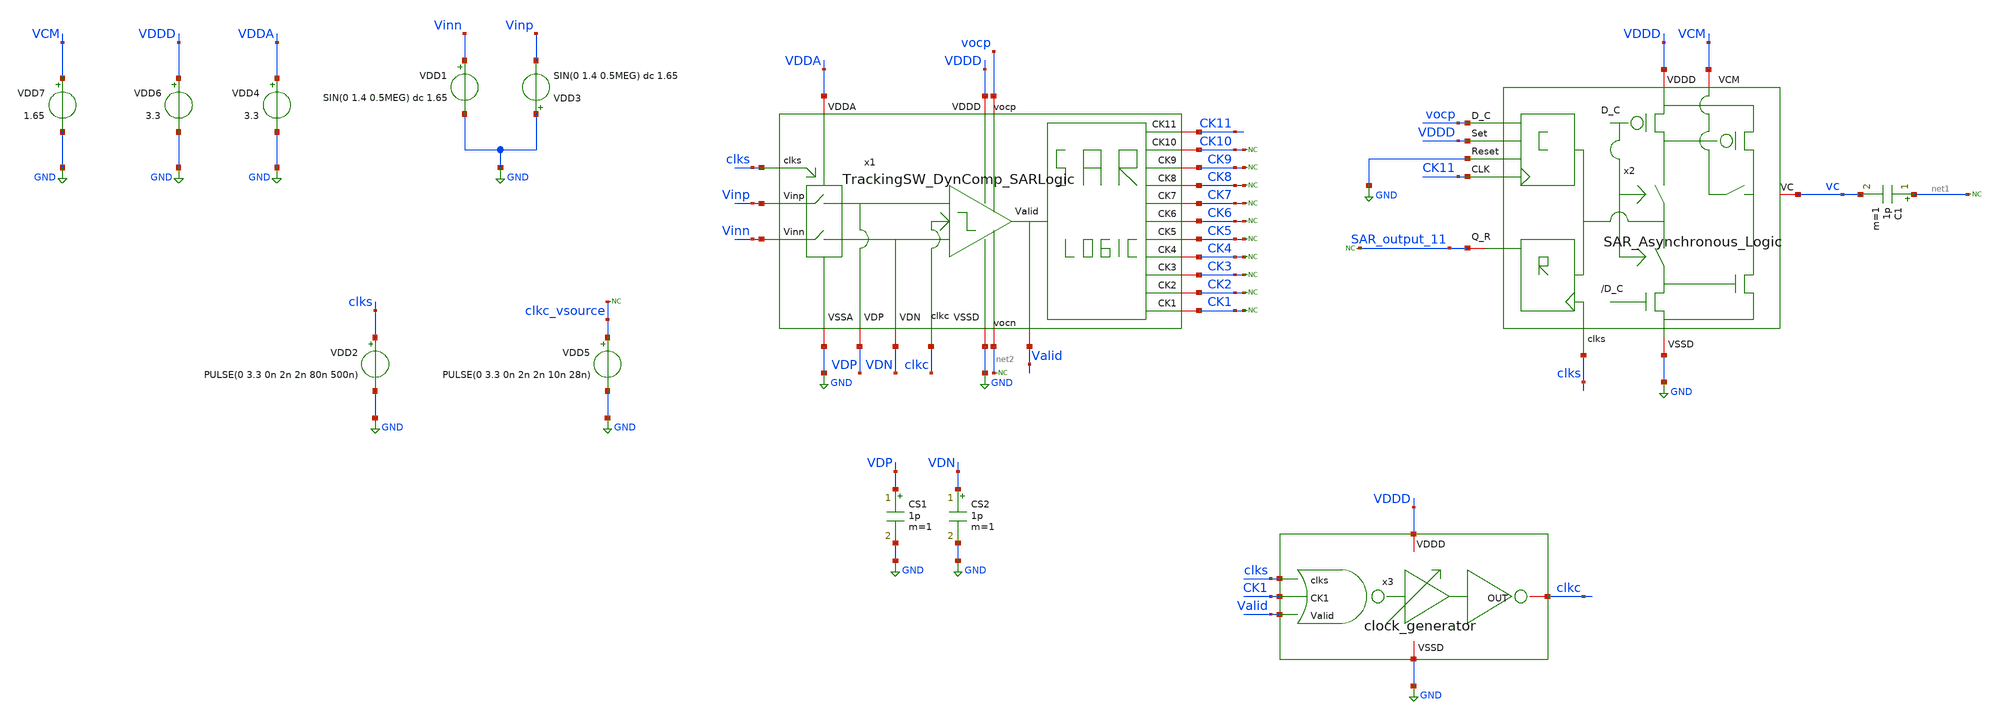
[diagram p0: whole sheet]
** sch_path: SAR_ADC/SAR_Asynchronous_Logic/xschem/SAR_Asynchronous_Logic_tb_ckp.sch
**.subckt SAR_Asynchronous_Logic_tb_ckp
VDD2 clks GND PULSE(0 3.3 0n 2n 2n 80n 500n)
VDD4 VDDA GND 3.3
VDD1 Vinn GND SIN(0 1.4 0.5MEG) dc 1.65
VDD3 GND Vinp SIN(0 1.4 0.5MEG) dc 1.65
VDD5 clkc_vsource GND PULSE(0 3.3 0n 2n 2n 10n 28n)
VDD6 VDDD GND 3.3
CS1 VDP GND 1p m=1
CS2 VDN GND 1p m=1
* noconn CK10
* noconn CK9
* noconn CK8
* noconn CK7
* noconn CK6
* noconn CK5
* noconn CK4
* noconn CK3
* noconn CK2
* noconn CK1
VDD7 VCM GND 1.65
x2 VCM vc SAR_output_11 clks VDDD GND VDDD GND vocp CK11 SAR_Asynchronous_Logic
* noconn #net1
* noconn #net2
x3 clkc VDDD GND clks CK1 Valid clock_generator
* noconn clkc_vsource
* noconn SAR_output_11
x1 Valid vocp net2 CK11 CK10 CK9 CK8 CK7 CK6 CK5 CK4 CK3 CK2 CK1 VDDA GND VDDD GND VDP clks VDN clkc
+ Vinp Vinn TrackingSW_DynComp_SARLogic
C1 net1 vc 1p m=1
**** begin user architecture code



*Parameters

.options TEMP = 50.0
.lib /home/electrica/Documents/gf180_projects/pdk/gf180mcuC/libs.tech/ngspice/sm141064.ngspice typical
.include /home/electrica/Documents/gf180_projects/pdk/gf180mcuC/libs.tech/ngspice/design.ngspice

*Data to save
.save all


* Simulation
.control
tran 0.1n 5u 0.01n
*setplot dc1
plot V(clkc_vsource)+16 V(clkc)+12 V(CK11)+8 V(vocp)+4 V(vc)
set filetype = ascii
write SAR_Asynchronous_Logic_tb_tran.raw

reset
unset filetype
op
save all
write SAR_Asynchronous_Logic_tb.raw


.endc
.end


**** end user architecture code
**.ends
.GLOBAL GND
.end
